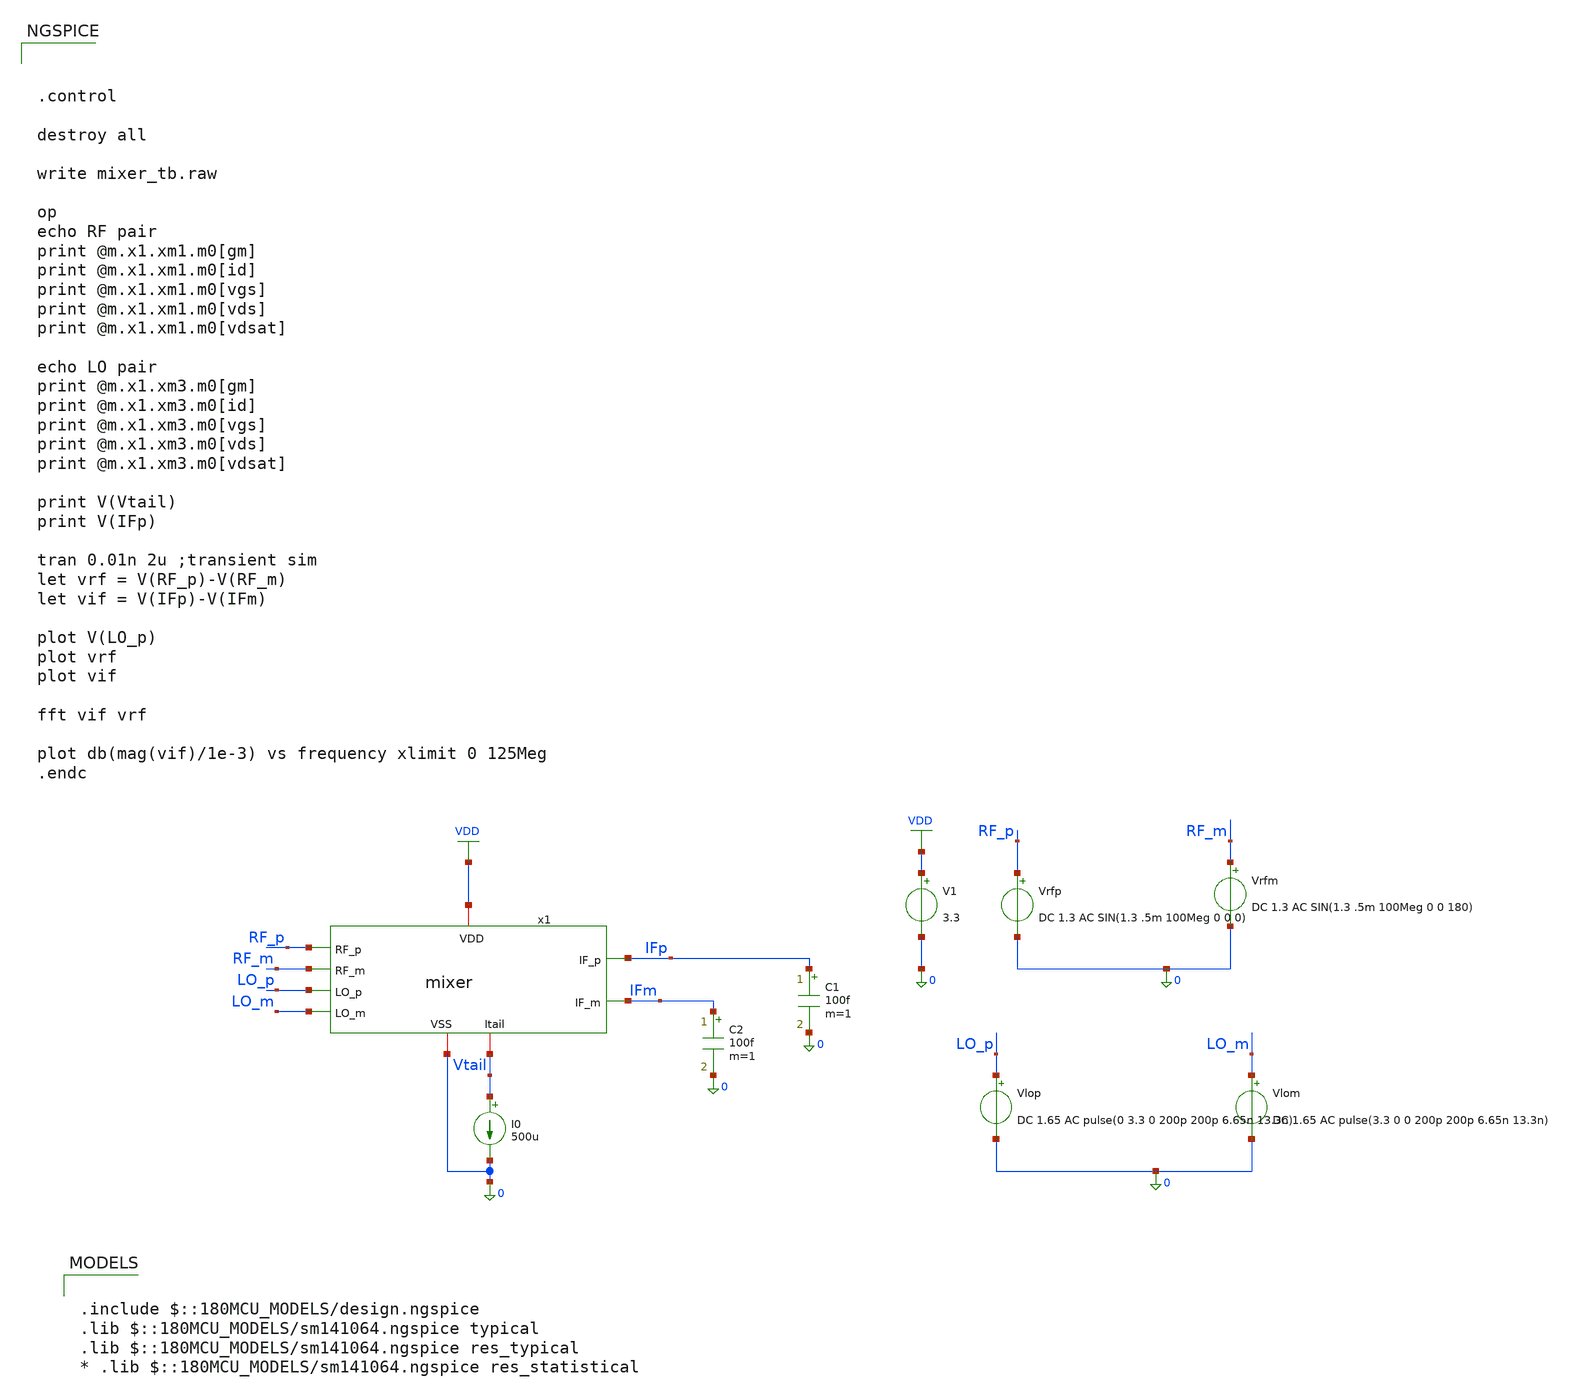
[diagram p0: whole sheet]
** sch_path: designs/mixer/testbench/mixer_tb.sch
**.subckt mixer_tb
V1 VDD 0 3.3
Vrfp RF_p 0 DC 1.3 AC SIN(1.3 .5m 100Meg 0 0 0)
Vrfm RF_m 0 DC 1.3 AC SIN(1.3 .5m 100Meg 0 0 180)
Vlop LO_p 0 DC 1.65 AC pulse(0 3.3 0 200p 200p 6.65n 13.3n)
Vlom LO_m 0 DC 1.65 AC pulse(3.3 0 0 200p 200p 6.65n 13.3n)
x1 IFp RF_p VDD 0 IFm RF_m LO_p Vtail LO_m mixer
I0 Vtail 0 500u
C1 IFp 0 100f m=1
C2 IFm 0 100f m=1
**** begin user architecture code

.include $::180MCU_MODELS/design.ngspice
.lib $::180MCU_MODELS/sm141064.ngspice typical
.lib $::180MCU_MODELS/sm141064.ngspice res_typical
* .lib $::180MCU_MODELS/sm141064.ngspice res_statistical




.control

destroy all

write mixer_tb.raw

op
echo RF pair
print @m.x1.xm1.m0[gm]
print @m.x1.xm1.m0[id]
print @m.x1.xm1.m0[vgs]
print @m.x1.xm1.m0[vds]
print @m.x1.xm1.m0[vdsat]

echo LO pair
print @m.x1.xm3.m0[gm]
print @m.x1.xm3.m0[id]
print @m.x1.xm3.m0[vgs]
print @m.x1.xm3.m0[vds]
print @m.x1.xm3.m0[vdsat]

print V(Vtail)
print V(IFp)

tran 0.01n 2u ;transient sim
let vrf = V(RF_p)-V(RF_m)
let vif = V(IFp)-V(IFm)

plot V(LO_p)
plot vrf
plot vif

fft vif vrf

plot db(mag(vif)/1e-3) vs frequency xlimit 0 125Meg
.endc


**** end user architecture code
**.ends

* expanding   symbol:  designs/mixer/schematic/mixer.sym # of pins=9
** sym_path: designs/mixer/schematic/mixer.sym
** sch_path: designs/mixer/schematic/mixer.sch
.subckt mixer IF_p RF_p VDD VSS IF_m RF_m LO_p Itail LO_m
*.iopin VDD
*.ipin LO_p
*.ipin LO_m
*.iopin Itail
*.opin IF_m
*.opin IF_p
*.iopin VSS
*.ipin RF_p
*.ipin RF_m
XM1 net1 RF_p Itail VSS nfet_03v3 L=0.28u W=36u nf=6 ad='int((nf+1)/2) * W/nf * 0.18u' as='int((nf+2)/2) * W/nf * 0.18u'
+ pd='2*int((nf+1)/2) * (W/nf + 0.18u)' ps='2*int((nf+2)/2) * (W/nf + 0.18u)' nrd='0.18u / W' nrs='0.18u / W'
+ sa=0 sb=0 sd=0 m=1
XM2 net2 RF_m Itail VSS nfet_03v3 L=0.28u W=36u nf=6 ad='int((nf+1)/2) * W/nf * 0.18u' as='int((nf+2)/2) * W/nf * 0.18u'
+ pd='2*int((nf+1)/2) * (W/nf + 0.18u)' ps='2*int((nf+2)/2) * (W/nf + 0.18u)' nrd='0.18u / W' nrs='0.18u / W'
+ sa=0 sb=0 sd=0 m=1
XM3 IF_m LO_p net1 VSS nfet_03v3 L=0.28u W=21u nf=7 ad='int((nf+1)/2) * W/nf * 0.18u' as='int((nf+2)/2) * W/nf * 0.18u'
+ pd='2*int((nf+1)/2) * (W/nf + 0.18u)' ps='2*int((nf+2)/2) * (W/nf + 0.18u)' nrd='0.18u / W' nrs='0.18u / W'
+ sa=0 sb=0 sd=0 m=1
XM4 IF_p LO_m net1 VSS nfet_03v3 L=0.28u W=21u nf=7 ad='int((nf+1)/2) * W/nf * 0.18u' as='int((nf+2)/2) * W/nf * 0.18u'
+ pd='2*int((nf+1)/2) * (W/nf + 0.18u)' ps='2*int((nf+2)/2) * (W/nf + 0.18u)' nrd='0.18u / W' nrs='0.18u / W'
+ sa=0 sb=0 sd=0 m=1
XM5 IF_m LO_m net2 VSS nfet_03v3 L=0.28u W=21u nf=7 ad='int((nf+1)/2) * W/nf * 0.18u' as='int((nf+2)/2) * W/nf * 0.18u'
+ pd='2*int((nf+1)/2) * (W/nf + 0.18u)' ps='2*int((nf+2)/2) * (W/nf + 0.18u)' nrd='0.18u / W' nrs='0.18u / W'
+ sa=0 sb=0 sd=0 m=1
XM6 IF_p LO_p net2 VSS nfet_03v3 L=0.28u W=21u nf=7 ad='int((nf+1)/2) * W/nf * 0.18u' as='int((nf+2)/2) * W/nf * 0.18u'
+ pd='2*int((nf+1)/2) * (W/nf + 0.18u)' ps='2*int((nf+2)/2) * (W/nf + 0.18u)' nrd='0.18u / W' nrs='0.18u / W'
+ sa=0 sb=0 sd=0 m=1
XR1 IF_p VDD VSS ppolyf_u_1k r_width=1e-6 r_length=7.4e-6 m=1
XR2 IF_m VDD VSS ppolyf_u_1k r_width=1e-6 r_length=7.4e-6 m=1
.ends

.GLOBAL VDD
.end
